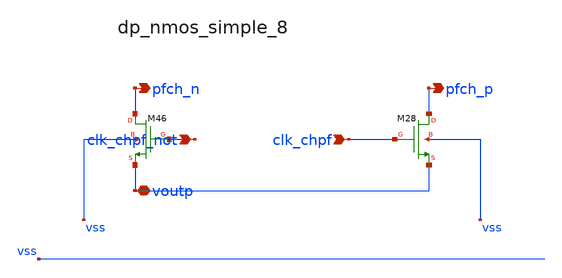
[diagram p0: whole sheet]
** sch_path: analog-db/raw/ia_003_fan_chopper_pf/hier/blocks/dp_nmos_simple_8.sch
**.subckt dp_nmos_simple_8 clk_chpf_not clk_chpf voutp pfch_n pfch_p
*.ipin clk_chpf_not
*.ipin clk_chpf
*.iopin voutp
*.opin pfch_n
*.opin pfch_p
XM28 pfch_p clk_chpf voutp vss sg13_lv_nmos w=x_dut_xm28_w l=x_dut_xm28_l ng=1 m=x_dut_xm28_m
XM46 pfch_n clk_chpf_not voutp vss sg13_lv_nmos w=x_dut_xm46_w l=x_dut_xm46_l ng=1 m=x_dut_xm46_m
**.ends
.end
